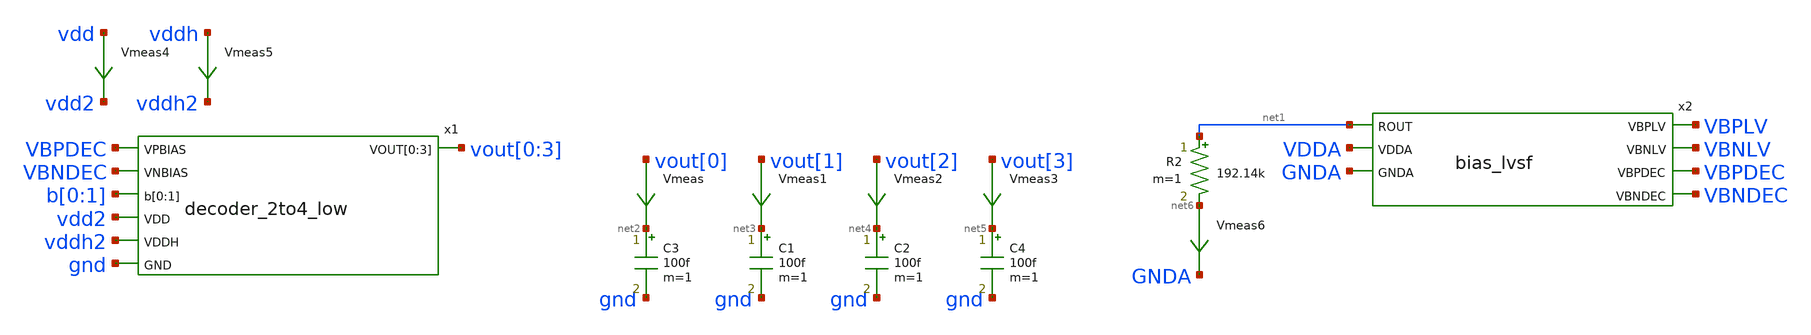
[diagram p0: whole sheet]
** sch_path: xschem/decoder_2to4-tb.sch
.lib $::SKYWATER_MODELS/sky130.lib.spice tt
.include $::SKYWATER_STDCELLS/sky130_fd_sc_hd.spice

**.subckt decoder_2to4-tb
Vmeas vout[0] net2 0
.save i(vmeas)
Vmeas1 vout[1] net3 0
.save i(vmeas1)
C3 net2 gnd 100f m=1
Vmeas2 vout[2] net4 0
.save i(vmeas2)
Vmeas3 vout[3] net5 0
.save i(vmeas3)
C1 net3 gnd 100f m=1
C2 net4 gnd 100f m=1
C4 net5 gnd 100f m=1
Vmeas4 vdd vdd2 0
.save i(vmeas4)
Vmeas5 vddh vddh2 0
.save i(vmeas5)
x1 VBPDEC VBNDEC b[0] b[1] vout[0] vout[1] vout[2] vout[3] vdd2 vddh2 gnd decoder_2to4_low
R2 net1 net6 192.14k m=1
Vmeas6 net6 GNDA 0
.save i(vmeas6)
x2 net1 VBPLV VBNLV VBPDEC VBNDEC VDDA GNDA bias_lvsf
**** begin user architecture code



  .option wnflag=1
  .option safecurrents
  .option klu
  ********************Static Voltage Sources***************************
  Vddh vddh gnd dc 5.5
  Vdd vdd gnd dc 1.8
  Vdda vdda gnd 5.5
  Vgnda gnda gnd 0
  .param vpb_val = 2.98 vnb_val=1.506

  *Vp vpbias gnd dc vpb_val
  *Vn vnbias gnd dc vnb_val
  ********************Dynamic Voltage Sources***************************
  *******Calculation**********
  .param base_f=100e3 base_t={1/base_f} base_th={base_t/2} base_d={base_th}
  .param d2_th ={base_th} d2_t={2*d2_th}
  .param d1_th ={4*d2_th} d1_t={d0_th}
  .param d0_th ={4*d1_th} d0_t={4*d0_th}

  .param d20_d ={0} d21_d={1*d2_th} d22_d={2*d2_th} d23_d={3*d2_th}
  .param d10_d ={0} d11_d={1*d1_th} d12_d={2*d1_th} d13_d={3*d1_th}
  .param d00_d ={0} d01_d={1*d0_th} d02_d={2*d0_th} d03_d={3*d0_th}
  *******Signals**********
  .param vhi=1.8
  Vin1 b[0] gnd pulse(0 {vhi} {0} 1p 1p {10u} {20u})
  Vin2 b[1] gnd pulse(0 {vhi} {0} 1p 1p {20u} {40u})

  *Vin1 b[0] gnd 0
  *vin2 b[1] gnd 0
  ********************Simulation Commands*****************************
  .control
     reset
     save all
     set num_threads=36
     tran 1n 100u
     write dec-tb.raw
     set appendwrite
*    quit 0
  .endc



**** end user architecture code
**.ends

* expanding   symbol:  decoder_2to4_low.sym # of pins=7
** sym_path: xschem/decoder_2to4_low.sym
** sch_path: xschem/decoder_2to4_low.sch
.subckt decoder_2to4_low VPBIAS VNBIAS b[0] b[1] VOUT[0] VOUT[1] VOUT[2] VOUT[3] VDD VDDH GND
*.ipin VPBIAS
*.ipin VNBIAS
*.ipin b[0],b[1]
*.opin VOUT[0],VOUT[1],VOUT[2],VOUT[3]
*.ipin VDDH
*.ipin GND
*.ipin VDD
x5 b[0] GND GND VDD VDD bb[0] sky130_fd_sc_hd__inv_1
x10 b[1] GND GND VDD VDD bb[1] sky130_fd_sc_hd__inv_1
x1 VPBIAS VNBIAS DIN[1] VOUT[0] VOUT[2] VOUT[3] VOUT[1] VDDH GND pd_network_parallel
x2 VPBIAS VNBIAS DIN[2] VOUT[0] VOUT[1] VOUT[3] VOUT[2] VDDH GND pd_network_parallel
x3 VPBIAS VNBIAS DIN[3] VOUT[0] VOUT[1] VOUT[2] VOUT[3] VDDH GND pd_network_parallel
x4 VPBIAS VNBIAS DIN[0] VOUT[1] VOUT[2] VOUT[3] VOUT[0] VDDH GND pd_network_parallel
x6 b[0] b[1] GND GND VDD VDD DIN[0] sky130_fd_sc_hd__nor2_1
x7 bb[0] b[1] GND GND VDD VDD DIN[1] sky130_fd_sc_hd__nor2_1
x8 b[0] bb[1] GND GND VDD VDD DIN[2] sky130_fd_sc_hd__nor2_1
x9 bb[0] bb[1] GND GND VDD VDD DIN[3] sky130_fd_sc_hd__nor2_1
.ends


* expanding   symbol:  bias_lvsf.sym # of pins=7
** sym_path: xschem/bias_lvsf.sym
** sch_path: xschem/bias_lvsf.sch
.subckt bias_lvsf ROUT VBPLV VBNLV VBPDEC VBNDEC VDDA GNDA
*.ipin ROUT
*.opin VBPLV
*.opin VBNLV
*.opin VBPDEC
*.opin VBNDEC
*.ipin VDDA
*.ipin GNDA
XM1 n1 n1 VDDA VDDA sky130_fd_pr__pfet_g5v0d10v5 L=lref W=wp_iref nf=1 ad='int((nf+1)/2) * W/nf * 0.29'
+ as='int((nf+2)/2) * W/nf * 0.29' pd='2*int((nf+1)/2) * (W/nf + 0.29)' ps='2*int((nf+2)/2) * (W/nf + 0.29)'
+ nrd='0.29 / W' nrs='0.29 / W' sa=0 sb=0 sd=0 mult=miref m=miref
.param wp_iref=1.8 wn_iref=0.6 miref=2 lref=4 lr=20
XM2 n2 n2 n1 VDDA sky130_fd_pr__pfet_g5v0d10v5 L=lref W=wp_iref nf=1 ad='int((nf+1)/2) * W/nf * 0.29'
+ as='int((nf+2)/2) * W/nf * 0.29' pd='2*int((nf+1)/2) * (W/nf + 0.29)' ps='2*int((nf+2)/2) * (W/nf + 0.29)'
+ nrd='0.29 / W' nrs='0.29 / W' sa=0 sb=0 sd=0 mult=miref m=miref
XR1 ROUT net1 GNDA sky130_fd_pr__res_xhigh_po_5p73 L=0.573 mult=1 m=1
XM3 net2 net1 n2 VDDA sky130_fd_pr__pfet_g5v0d10v5 L=lr W=wp_iref nf=1 ad='int((nf+1)/2) * W/nf * 0.29'
+ as='int((nf+2)/2) * W/nf * 0.29' pd='2*int((nf+1)/2) * (W/nf + 0.29)' ps='2*int((nf+2)/2) * (W/nf + 0.29)'
+ nrd='0.29 / W' nrs='0.29 / W' sa=0 sb=0 sd=0 mult=miref m=miref
XM4 net1 net1 net2 VDDA sky130_fd_pr__pfet_g5v0d10v5 L=lr W=wp_iref nf=1 ad='int((nf+1)/2) * W/nf * 0.29'
+ as='int((nf+2)/2) * W/nf * 0.29' pd='2*int((nf+1)/2) * (W/nf + 0.29)' ps='2*int((nf+2)/2) * (W/nf + 0.29)'
+ nrd='0.29 / W' nrs='0.29 / W' sa=0 sb=0 sd=0 mult=miref m=miref
XM5 net3 n1 VDDA VDDA sky130_fd_pr__pfet_g5v0d10v5 L=lref W=wp_iref nf=1 ad='int((nf+1)/2) * W/nf * 0.29'
+ as='int((nf+2)/2) * W/nf * 0.29' pd='2*int((nf+1)/2) * (W/nf + 0.29)' ps='2*int((nf+2)/2) * (W/nf + 0.29)'
+ nrd='0.29 / W' nrs='0.29 / W' sa=0 sb=0 sd=0 mult=miref m=miref
XM6 n3 n2 net3 VDDA sky130_fd_pr__pfet_g5v0d10v5 L=lref W=wp_iref nf=1 ad='int((nf+1)/2) * W/nf * 0.29'
+ as='int((nf+2)/2) * W/nf * 0.29' pd='2*int((nf+1)/2) * (W/nf + 0.29)' ps='2*int((nf+2)/2) * (W/nf + 0.29)'
+ nrd='0.29 / W' nrs='0.29 / W' sa=0 sb=0 sd=0 mult=miref m=miref
Vmeas1 net8 GNDA 0
.save i(vmeas1)
XM7 n3 n3 n4 GNDA sky130_fd_pr__nfet_g5v0d10v5 L=lref W=wn_iref nf=1 ad='int((nf+1)/2) * W/nf * 0.29'
+ as='int((nf+2)/2) * W/nf * 0.29' pd='2*int((nf+1)/2) * (W/nf + 0.29)' ps='2*int((nf+2)/2) * (W/nf + 0.29)'
+ nrd='0.29 / W' nrs='0.29 / W' sa=0 sb=0 sd=0 mult=miref m=miref
XM8 n4 n4 net8 GNDA sky130_fd_pr__nfet_g5v0d10v5 L=lref W=wn_iref nf=1 ad='int((nf+1)/2) * W/nf * 0.29'
+ as='int((nf+2)/2) * W/nf * 0.29' pd='2*int((nf+1)/2) * (W/nf + 0.29)' ps='2*int((nf+2)/2) * (W/nf + 0.29)'
+ nrd='0.29 / W' nrs='0.29 / W' sa=0 sb=0 sd=0 mult=miref m=miref
XM9 net4 n1 VDDA VDDA sky130_fd_pr__pfet_g5v0d10v5 L=lref W=wp_iref nf=1 ad='int((nf+1)/2) * W/nf * 0.29'
+ as='int((nf+2)/2) * W/nf * 0.29' pd='2*int((nf+1)/2) * (W/nf + 0.29)' ps='2*int((nf+2)/2) * (W/nf + 0.29)'
+ nrd='0.29 / W' nrs='0.29 / W' sa=0 sb=0 sd=0 mult=miref m=miref
XM10 VBNLV n2 net4 VDDA sky130_fd_pr__pfet_g5v0d10v5 L=lref W=wp_iref nf=1 ad='int((nf+1)/2) * W/nf * 0.29'
+ as='int((nf+2)/2) * W/nf * 0.29' pd='2*int((nf+1)/2) * (W/nf + 0.29)' ps='2*int((nf+2)/2) * (W/nf + 0.29)'
+ nrd='0.29 / W' nrs='0.29 / W' sa=0 sb=0 sd=0 mult=miref m=miref
XM11 net5 n1 VDDA VDDA sky130_fd_pr__pfet_g5v0d10v5 L=lref W=wp_iref nf=1 ad='int((nf+1)/2) * W/nf * 0.29'
+ as='int((nf+2)/2) * W/nf * 0.29' pd='2*int((nf+1)/2) * (W/nf + 0.29)' ps='2*int((nf+2)/2) * (W/nf + 0.29)'
+ nrd='0.29 / W' nrs='0.29 / W' sa=0 sb=0 sd=0 mult=miref m=miref
XM12 VBNDEC n2 net5 VDDA sky130_fd_pr__pfet_g5v0d10v5 L=lref W=wp_iref nf=1 ad='int((nf+1)/2) * W/nf * 0.29'
+ as='int((nf+2)/2) * W/nf * 0.29' pd='2*int((nf+1)/2) * (W/nf + 0.29)' ps='2*int((nf+2)/2) * (W/nf + 0.29)'
+ nrd='0.29 / W' nrs='0.29 / W' sa=0 sb=0 sd=0 mult=miref m=miref
XM13 VBNLV VBNLV n6 GNDA sky130_fd_pr__nfet_g5v0d10v5 L=lref W=wn_iref nf=1 ad='int((nf+1)/2) * W/nf * 0.29'
+ as='int((nf+2)/2) * W/nf * 0.29' pd='2*int((nf+1)/2) * (W/nf + 0.29)' ps='2*int((nf+2)/2) * (W/nf + 0.29)'
+ nrd='0.29 / W' nrs='0.29 / W' sa=0 sb=0 sd=0 mult=miref m=miref
XM14 n6 VBNLV net9 GNDA sky130_fd_pr__nfet_g5v0d10v5 L=5.3 W=0.6 nf=1 ad='int((nf+1)/2) * W/nf * 0.29'
+ as='int((nf+2)/2) * W/nf * 0.29' pd='2*int((nf+1)/2) * (W/nf + 0.29)' ps='2*int((nf+2)/2) * (W/nf + 0.29)'
+ nrd='0.29 / W' nrs='0.29 / W' sa=0 sb=0 sd=0 mult=1 m=1
Vmeas2 net9 GNDA 0
.save i(vmeas2)
XM15 VBNDEC VBNDEC n7 GNDA sky130_fd_pr__nfet_g5v0d10v5 L=lref W=wn_iref nf=1 ad='int((nf+1)/2) * W/nf * 0.29'
+ as='int((nf+2)/2) * W/nf * 0.29' pd='2*int((nf+1)/2) * (W/nf + 0.29)' ps='2*int((nf+2)/2) * (W/nf + 0.29)'
+ nrd='0.29 / W' nrs='0.29 / W' sa=0 sb=0 sd=0 mult=miref m=miref
XM16 n7 VBNDEC net10 GNDA sky130_fd_pr__nfet_g5v0d10v5 L=9.7 W=0.61 nf=1 ad='int((nf+1)/2) * W/nf * 0.29'
+ as='int((nf+2)/2) * W/nf * 0.29' pd='2*int((nf+1)/2) * (W/nf + 0.29)' ps='2*int((nf+2)/2) * (W/nf + 0.29)'
+ nrd='0.29 / W' nrs='0.29 / W' sa=0 sb=0 sd=0 mult=1 m=1
Vmeas3 net10 GNDA 0
.save i(vmeas3)
XM17 n10 VBPLV VDDA VDDA sky130_fd_pr__pfet_g5v0d10v5 L=9.2 W=1 nf=1 ad='int((nf+1)/2) * W/nf * 0.29'
+ as='int((nf+2)/2) * W/nf * 0.29' pd='2*int((nf+1)/2) * (W/nf + 0.29)' ps='2*int((nf+2)/2) * (W/nf + 0.29)'
+ nrd='0.29 / W' nrs='0.29 / W' sa=0 sb=0 sd=0 mult=1 m=1
XM18 VBPLV VBPLV n10 VDDA sky130_fd_pr__pfet_g5v0d10v5 L=lref W=wp_iref nf=1 ad='int((nf+1)/2) * W/nf * 0.29'
+ as='int((nf+2)/2) * W/nf * 0.29' pd='2*int((nf+1)/2) * (W/nf + 0.29)' ps='2*int((nf+2)/2) * (W/nf + 0.29)'
+ nrd='0.29 / W' nrs='0.29 / W' sa=0 sb=0 sd=0 mult=miref m=miref
Vmeas4 net11 GNDA 0
.save i(vmeas4)
XM19 VBPLV n3 net6 GNDA sky130_fd_pr__nfet_g5v0d10v5 L=lref W=wn_iref nf=1 ad='int((nf+1)/2) * W/nf * 0.29'
+ as='int((nf+2)/2) * W/nf * 0.29' pd='2*int((nf+1)/2) * (W/nf + 0.29)' ps='2*int((nf+2)/2) * (W/nf + 0.29)'
+ nrd='0.29 / W' nrs='0.29 / W' sa=0 sb=0 sd=0 mult=miref m=miref
XM20 net6 n4 net11 GNDA sky130_fd_pr__nfet_g5v0d10v5 L=lref W=wn_iref nf=1 ad='int((nf+1)/2) * W/nf * 0.29'
+ as='int((nf+2)/2) * W/nf * 0.29' pd='2*int((nf+1)/2) * (W/nf + 0.29)' ps='2*int((nf+2)/2) * (W/nf + 0.29)'
+ nrd='0.29 / W' nrs='0.29 / W' sa=0 sb=0 sd=0 mult=miref m=miref
XM26 net7 n1 VDDA VDDA sky130_fd_pr__pfet_g5v0d10v5 L=lref W=wp_iref nf=1 ad='int((nf+1)/2) * W/nf * 0.29'
+ as='int((nf+2)/2) * W/nf * 0.29' pd='2*int((nf+1)/2) * (W/nf + 0.29)' ps='2*int((nf+2)/2) * (W/nf + 0.29)'
+ nrd='0.29 / W' nrs='0.29 / W' sa=0 sb=0 sd=0 mult=miref m=miref
XM27 VBPDEC n2 net7 VDDA sky130_fd_pr__pfet_g5v0d10v5 L=lref W=wp_iref nf=1 ad='int((nf+1)/2) * W/nf * 0.29'
+ as='int((nf+2)/2) * W/nf * 0.29' pd='2*int((nf+1)/2) * (W/nf + 0.29)' ps='2*int((nf+2)/2) * (W/nf + 0.29)'
+ nrd='0.29 / W' nrs='0.29 / W' sa=0 sb=0 sd=0 mult=miref m=miref
XM28 VBPDEC VBPDEC n14 GNDA sky130_fd_pr__nfet_g5v0d10v5 L=lref W=wn_iref nf=1 ad='int((nf+1)/2) * W/nf * 0.29'
+ as='int((nf+2)/2) * W/nf * 0.29' pd='2*int((nf+1)/2) * (W/nf + 0.29)' ps='2*int((nf+2)/2) * (W/nf + 0.29)'
+ nrd='0.29 / W' nrs='0.29 / W' sa=0 sb=0 sd=0 mult=miref m=miref
XM29 n14 n14 net12 GNDA sky130_fd_pr__nfet_g5v0d10v5 L=12 W=0.64 nf=1 ad='int((nf+1)/2) * W/nf * 0.29'
+ as='int((nf+2)/2) * W/nf * 0.29' pd='2*int((nf+1)/2) * (W/nf + 0.29)' ps='2*int((nf+2)/2) * (W/nf + 0.29)'
+ nrd='0.29 / W' nrs='0.29 / W' sa=0 sb=0 sd=0 mult=1 m=1
Vmeas6 net12 GNDA 0
.save i(vmeas6)
.ends


* expanding   symbol:  pd_network_parallel.sym # of pins=7
** sym_path: xschem/pd_network_parallel.sym
** sch_path: xschem/pd_network_parallel.sch
.subckt pd_network_parallel VPBIAS VNBIAS DIN V[0] V[1] V[2] VOUT VDDH GND
*.ipin VPBIAS
*.ipin VNBIAS
*.ipin DIN
*.ipin V[0],V[1],V[2]
*.opin VOUT
*.ipin VDDH
*.ipin GND
.param wp=0.84 wn=1 l=1

XM1 net1 VPBIAS VDDH VDDH sky130_fd_pr__pfet_g5v0d10v5 L=l W=wp nf=1 ad='int((nf+1)/2) * W/nf * 0.29'
+ as='int((nf+2)/2) * W/nf * 0.29' pd='2*int((nf+1)/2) * (W/nf + 0.29)' ps='2*int((nf+2)/2) * (W/nf + 0.29)'
+ nrd='0.29 / W' nrs='0.29 / W' sa=0 sb=0 sd=0 mult=1 m=1
XM5 VOUT VNBIAS net2 GND sky130_fd_pr__nfet_g5v0d10v5 L=l W=wn nf=1 ad='int((nf+1)/2) * W/nf * 0.29'
+ as='int((nf+2)/2) * W/nf * 0.29' pd='2*int((nf+1)/2) * (W/nf + 0.29)' ps='2*int((nf+2)/2) * (W/nf + 0.29)'
+ nrd='0.29 / W' nrs='0.29 / W' sa=0 sb=0 sd=0 mult=1 m=1
XM2 VOUT V[0] net1 VDDH sky130_fd_pr__pfet_g5v0d10v5 L=l W=wp nf=1 ad='int((nf+1)/2) * W/nf * 0.29' as='int((nf+2)/2) * W/nf * 0.29'
+ pd='2*int((nf+1)/2) * (W/nf + 0.29)' ps='2*int((nf+2)/2) * (W/nf + 0.29)' nrd='0.29 / W' nrs='0.29 / W'
+ sa=0 sb=0 sd=0 mult=1 m=1
XM3 VOUT V[1] net1 VDDH sky130_fd_pr__pfet_g5v0d10v5 L=l W=wp nf=1 ad='int((nf+1)/2) * W/nf * 0.29' as='int((nf+2)/2) * W/nf * 0.29'
+ pd='2*int((nf+1)/2) * (W/nf + 0.29)' ps='2*int((nf+2)/2) * (W/nf + 0.29)' nrd='0.29 / W' nrs='0.29 / W'
+ sa=0 sb=0 sd=0 mult=1 m=1
XM4 VOUT V[2] net1 VDDH sky130_fd_pr__pfet_g5v0d10v5 L=l W=wp nf=1 ad='int((nf+1)/2) * W/nf * 0.29' as='int((nf+2)/2) * W/nf * 0.29'
+ pd='2*int((nf+1)/2) * (W/nf + 0.29)' ps='2*int((nf+2)/2) * (W/nf + 0.29)' nrd='0.29 / W' nrs='0.29 / W'
+ sa=0 sb=0 sd=0 mult=1 m=1
XM6 net2 DIN GND GND sky130_fd_pr__nfet_01v8 L=0.15 W=2 nf=1 ad='int((nf+1)/2) * W/nf * 0.29' as='int((nf+2)/2) * W/nf * 0.29'
+ pd='2*int((nf+1)/2) * (W/nf + 0.29)' ps='2*int((nf+2)/2) * (W/nf + 0.29)' nrd='0.29 / W' nrs='0.29 / W'
+ sa=0 sb=0 sd=0 mult=1 m=1
.ends

.end
